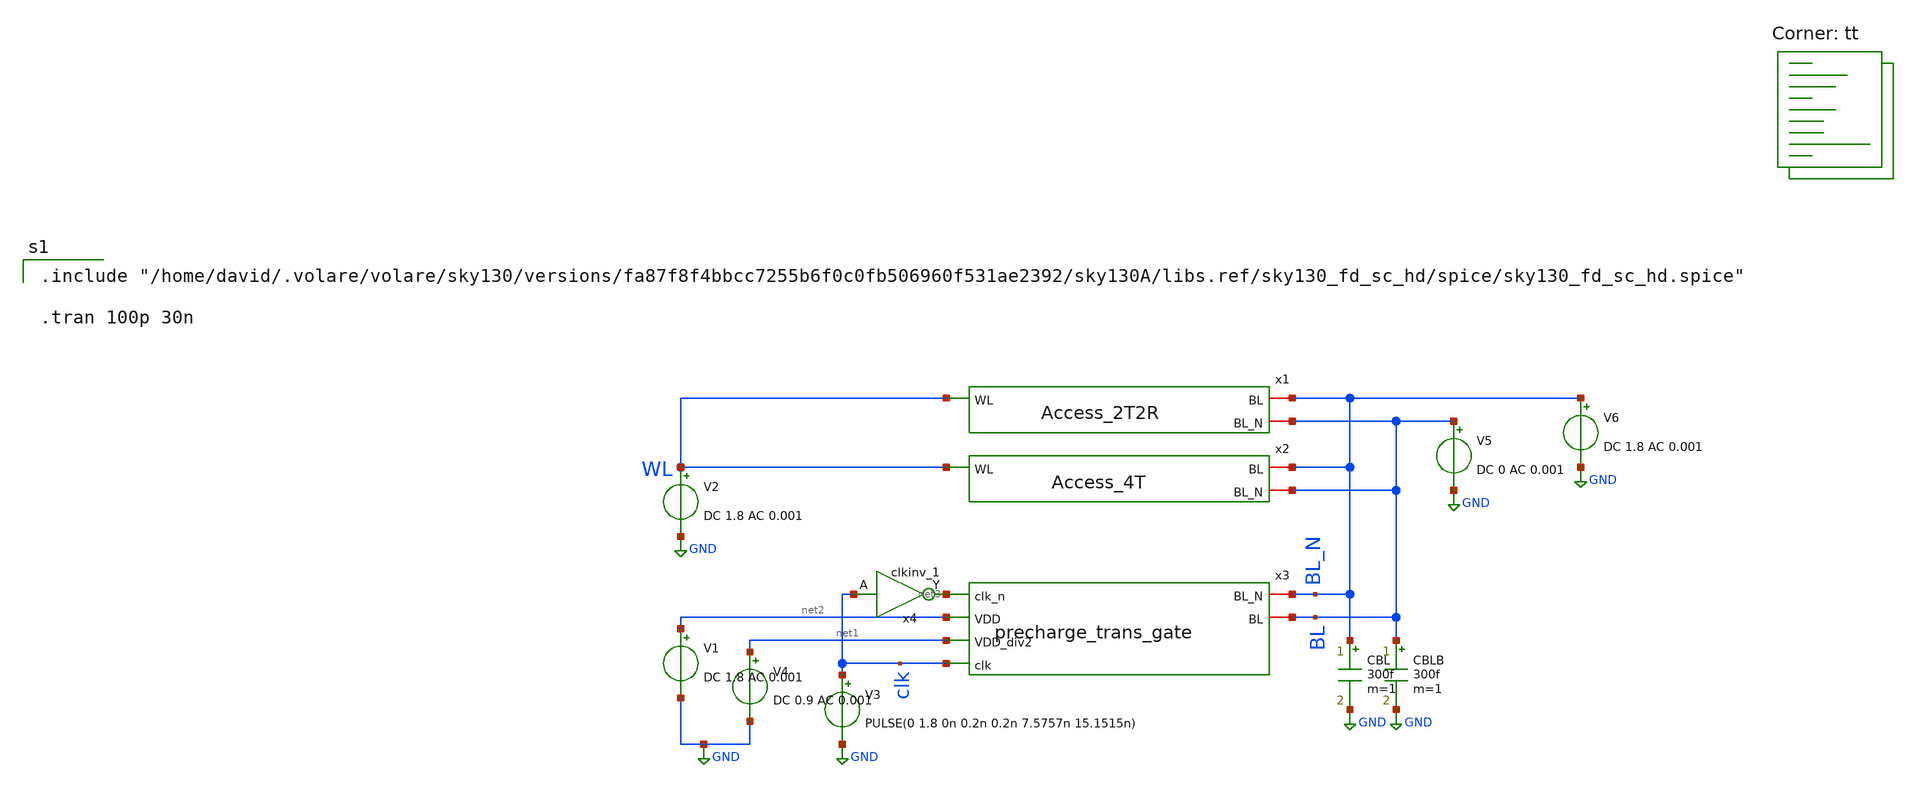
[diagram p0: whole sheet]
** sch_path: analog/schematics/write_tb.sch
**.subckt write_tb
x1 WL BL_N BL Access_2T2R
x2 WL BL_N BL Access_4T
x3 net3 BL_N BL net2 net1 clk precharge_trans_gate
V3 clk GND PULSE(0 1.8 0n 0.2n 0.2n 7.5757n 15.1515n)
x4 clk VGND VNB VPB VPWR net3 sky130_fd_sc_hd__clkinv_1
V4 net1 GND DC 0.9 AC 0.001
V1 net2 GND DC 1.8 AC 0.001
V2 WL GND DC 1.8 AC 0.001
CBLB BL GND 300f m=1
CBL BL_N GND 300f m=1
V5 BL GND DC 0 AC 0.001
V6 BL_N GND DC 1.8 AC 0.001
**** begin user architecture code
.lib $::SKYWATER_MODELS/sky130.lib.spice tt

.include "/home/david/.volare/volare/sky130/versions/fa87f8f4bbcc7255b6f0c0fb506960f531ae2392/sky130A/libs.ref/sky130_fd_sc_hd/spice/sky130_fd_sc_hd.spice"

.tran 100p 30n

**** end user architecture code
**.ends
.GLOBAL GND
.end
